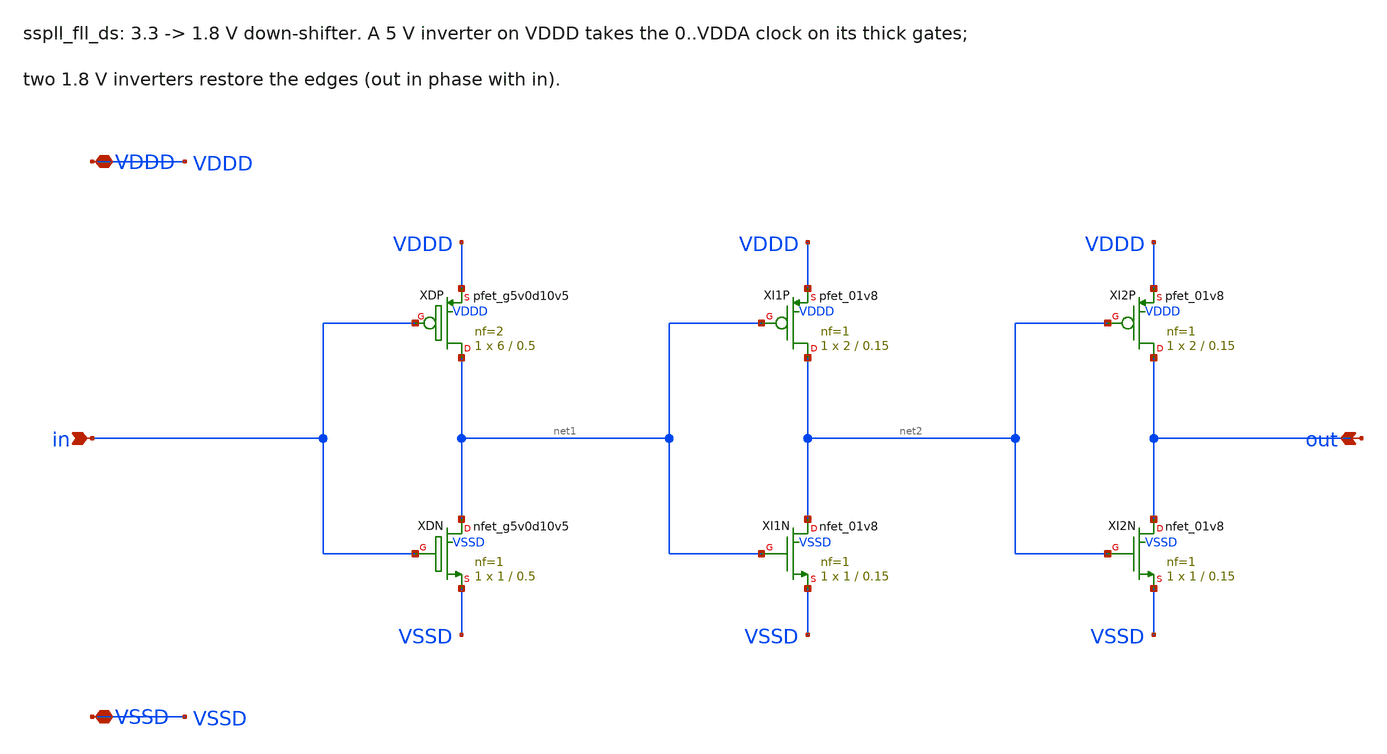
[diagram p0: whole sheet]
** sch_path: xschem/fll_hv/sspll_fll_ds.sch
**.subckt sspll_fll_ds in out VDDD VSSD
*.ipin in
*.opin out
*.iopin VDDD
*.iopin VSSD
XXDP net1 in VDDD VDDD sky130_fd_pr__pfet_g5v0d10v5 L=0.5 W=6 nf=2 ad='int((nf+1)/2) * W/nf * 0.29' as='int((nf+2)/2) * W/nf * 0.29'
+ pd='2*int((nf+1)/2) * (W/nf + 0.29)' ps='2*int((nf+2)/2) * (W/nf + 0.29)' nrd='0.29 / W' nrs='0.29 / W'
+ sa=0 sb=0 sd=0 mult=1 m=1
XXDN net1 in VSSD VSSD sky130_fd_pr__nfet_g5v0d10v5 L=0.5 W=1 nf=1 ad='int((nf+1)/2) * W/nf * 0.29' as='int((nf+2)/2) * W/nf * 0.29'
+ pd='2*int((nf+1)/2) * (W/nf + 0.29)' ps='2*int((nf+2)/2) * (W/nf + 0.29)' nrd='0.29 / W' nrs='0.29 / W'
+ sa=0 sb=0 sd=0 mult=1 m=1
XXI1P net2 net1 VDDD VDDD sky130_fd_pr__pfet_01v8 L=0.15 W=2 nf=1 ad='int((nf+1)/2) * W/nf * 0.29' as='int((nf+2)/2) * W/nf * 0.29'
+ pd='2*int((nf+1)/2) * (W/nf + 0.29)' ps='2*int((nf+2)/2) * (W/nf + 0.29)' nrd='0.29 / W' nrs='0.29 / W'
+ sa=0 sb=0 sd=0 mult=1 m=1
XXI1N net2 net1 VSSD VSSD sky130_fd_pr__nfet_01v8 L=0.15 W=1 nf=1 ad='int((nf+1)/2) * W/nf * 0.29' as='int((nf+2)/2) * W/nf * 0.29'
+ pd='2*int((nf+1)/2) * (W/nf + 0.29)' ps='2*int((nf+2)/2) * (W/nf + 0.29)' nrd='0.29 / W' nrs='0.29 / W'
+ sa=0 sb=0 sd=0 mult=1 m=1
XXI2P out net2 VDDD VDDD sky130_fd_pr__pfet_01v8 L=0.15 W=2 nf=1 ad='int((nf+1)/2) * W/nf * 0.29' as='int((nf+2)/2) * W/nf * 0.29'
+ pd='2*int((nf+1)/2) * (W/nf + 0.29)' ps='2*int((nf+2)/2) * (W/nf + 0.29)' nrd='0.29 / W' nrs='0.29 / W'
+ sa=0 sb=0 sd=0 mult=1 m=1
XXI2N out net2 VSSD VSSD sky130_fd_pr__nfet_01v8 L=0.15 W=1 nf=1 ad='int((nf+1)/2) * W/nf * 0.29' as='int((nf+2)/2) * W/nf * 0.29'
+ pd='2*int((nf+1)/2) * (W/nf + 0.29)' ps='2*int((nf+2)/2) * (W/nf + 0.29)' nrd='0.29 / W' nrs='0.29 / W'
+ sa=0 sb=0 sd=0 mult=1 m=1
**.ends
.end
